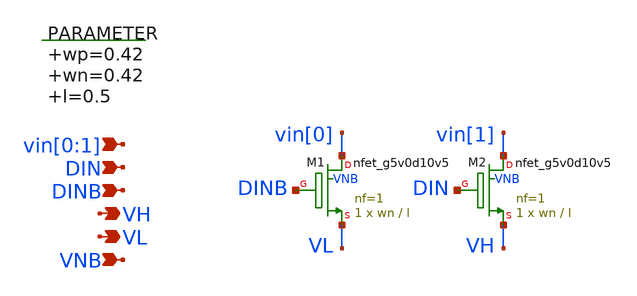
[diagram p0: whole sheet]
** sch_path: xschem/switch_nmos_2g_2o.sch
**.subckt switch_nmos_2g_2o vin[0],vin[1] VH VNB DIN VL DINB
*.ipin vin[0],vin[1]
*.opin VH
*.ipin VNB
*.ipin DIN
*.opin VL
*.ipin DINB
.param wp=0.42 wn=0.42 l=0.5

XM2 vin[1] DIN VH VNB sky130_fd_pr__nfet_g5v0d10v5 L=l W=wn nf=1 ad='int((nf+1)/2) * W/nf * 0.29' as='int((nf+2)/2) * W/nf * 0.29'
+ pd='2*int((nf+1)/2) * (W/nf + 0.29)' ps='2*int((nf+2)/2) * (W/nf + 0.29)' nrd='0.29 / W' nrs='0.29 / W'
+ sa=0 sb=0 sd=0 mult=1 m=1
XM1 vin[0] DINB VL VNB sky130_fd_pr__nfet_g5v0d10v5 L=l W=wn nf=1 ad='int((nf+1)/2) * W/nf * 0.29' as='int((nf+2)/2) * W/nf * 0.29'
+ pd='2*int((nf+1)/2) * (W/nf + 0.29)' ps='2*int((nf+2)/2) * (W/nf + 0.29)' nrd='0.29 / W' nrs='0.29 / W'
+ sa=0 sb=0 sd=0 mult=1 m=1
**.ends
.end
